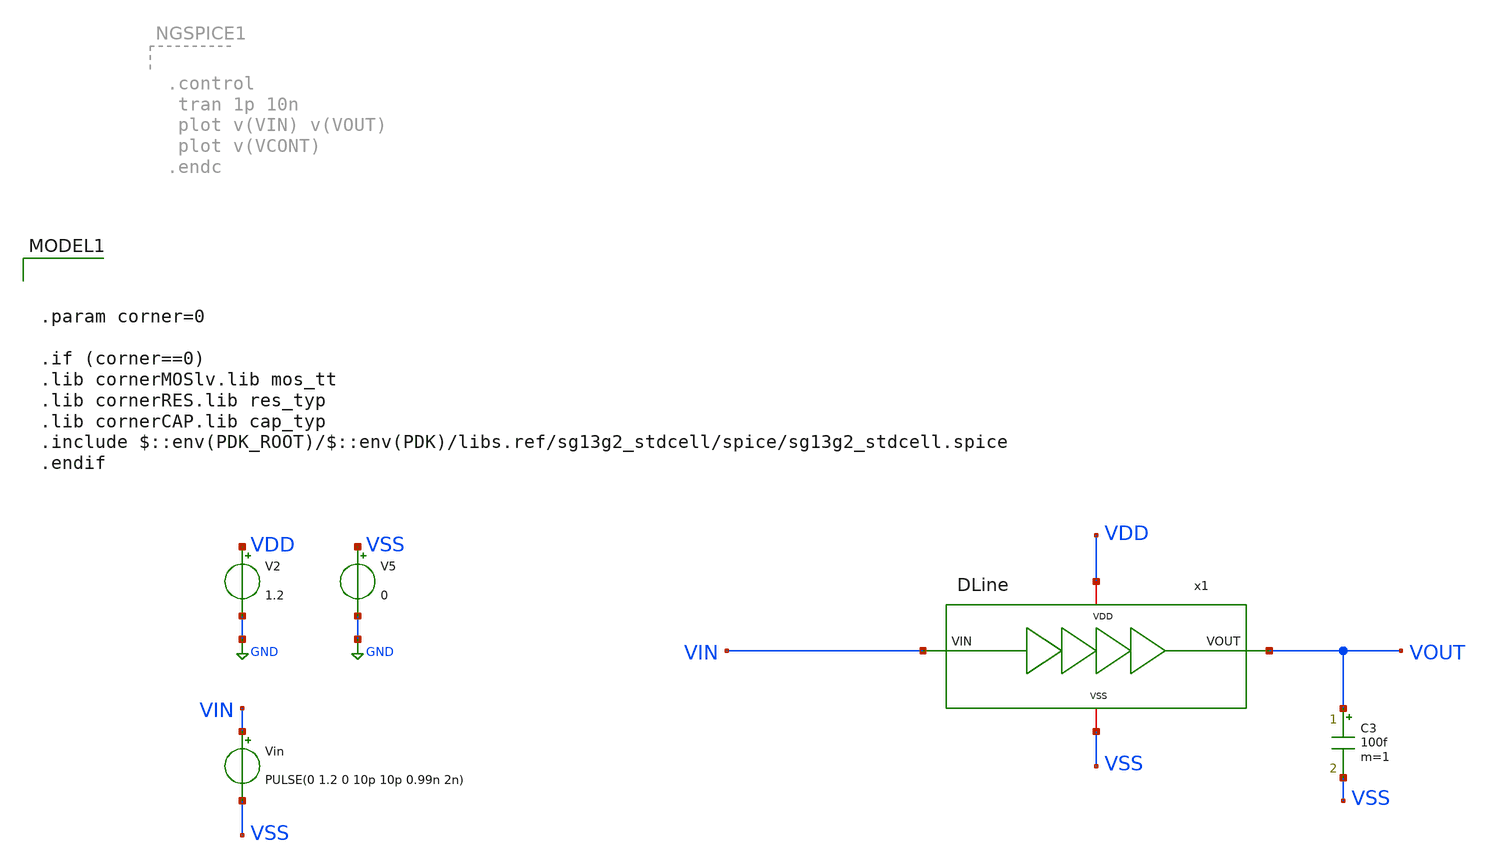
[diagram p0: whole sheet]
** sch_path: QDLL6501-main/schematic/xschem/testbenches/tb_large_delay.sch
**.subckt tb_large_delay
Vin VIN VSS PULSE(0 1.2 0 10p 10p 0.99n 2n)
C3 VOUT VSS 100f m=1
V2 VDD GND 1.2
V5 VSS GND 0
x1 VSS VDD VIN VOUT DLine
**** begin user architecture code


.param corner=0

.if (corner==0)
.lib cornerMOSlv.lib mos_tt
.lib cornerRES.lib res_typ
.lib cornerCAP.lib cap_typ
.include $::env(PDK_ROOT)/$::env(PDK)/libs.ref/sg13g2_stdcell/spice/sg13g2_stdcell.spice
.endif



.control
* ---- settings you tweak ----


   * ---- user settings ----
  let vlow  = 0
  let vhigh = 1.2
  let v50   = vlow + 0.5*(vhigh - vlow)

  let start_edge = 0     ; skip early edges (settling)
  let N = 200             ; number of phase samples



  tran 2p 200n

  * ---- allocate vectors ----
  let tvec   = vector(N)
  let phivec = vector(N)

  let k = 0
  let i = start_edge

  while k < N
    * crossing times
    meas tran tin      WHEN v(VIN)=v50  RISE=i
    meas tran tout     WHEN v(VOUT)=v50 RISE=i
    meas tran tin_next WHEN v(VIN)=v50  RISE=(i+1)

    * delay + period
    let dt = tout - tin
    let T  = tin_next - tin

    * phase in degrees (per-cycle)
    let phi = 360*dt/T
    let phi = phi - 360*floor(phi/360)

    * store sample at time = tin
    let tvec[k]   = tin
    let phivec[k] = phi

    let k = k + 1
    let i = i + 1
  end

  * plot phase vs time (one point per cycle)
  plot phivec vs tvec
  *plot v(VCONT)
  plot v(VIN) v(VOUT)
.endc


**** end user architecture code
**.ends
.GLOBAL GND
.end
